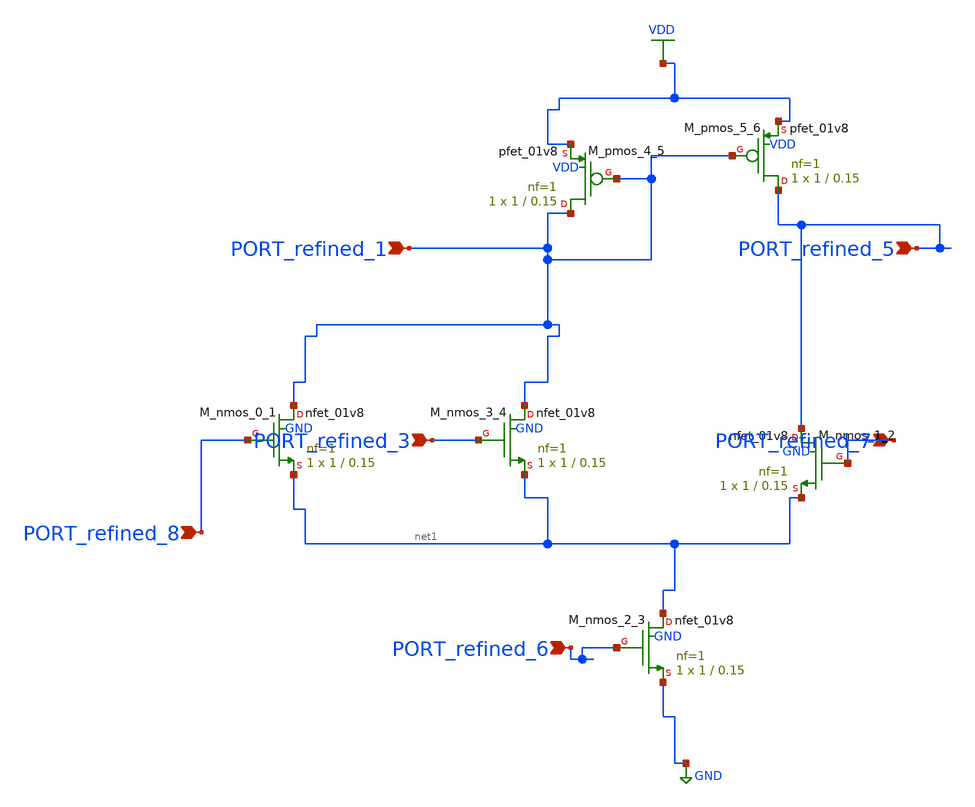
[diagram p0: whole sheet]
** sch_path: schematics/SchemGen/10_1109_TCSI_2022_3216201_04_001_crop1.sch
**.subckt 10_1109_TCSI_2022_3216201_04_001_crop1 PORT_refined_5 PORT_refined_6 PORT_refined_1
*+ PORT_refined_7 PORT_refined_8 PORT_refined_3
*.ipin PORT_refined_5
*.ipin PORT_refined_6
*.ipin PORT_refined_1
*.ipin PORT_refined_7
*.ipin PORT_refined_8
*.ipin PORT_refined_3
XM_nmos_0_1 PORT_refined_1 PORT_refined_8 net1 GND sky130_fd_pr__nfet_01v8 L=0.15 W=1 nf=1 ad='int((1 + 1)/2) * 1 / 1 * 0.29'
+ as='int((1 + 2)/2) * 1 / 1 * 0.29' pd='2*int((1 + 1)/2) * (1 / 1 + 0.29)' ps='2*int((1 + 2)/2) * (1 / 1 + 0.29)'
+ nrd='0.29 / 1 ' nrs='0.29 / 1 ' sa=0 sb=0 sd=0 mult=1 m=1
XM_nmos_1_2 PORT_refined_5 PORT_refined_7 net1 GND sky130_fd_pr__nfet_01v8 L=0.15 W=1 nf=1 ad='int((1 + 1)/2) * 1 / 1 * 0.29'
+ as='int((1 + 2)/2) * 1 / 1 * 0.29' pd='2*int((1 + 1)/2) * (1 / 1 + 0.29)' ps='2*int((1 + 2)/2) * (1 / 1 + 0.29)'
+ nrd='0.29 / 1 ' nrs='0.29 / 1 ' sa=0 sb=0 sd=0 mult=1 m=1
XM_nmos_2_3 net1 PORT_refined_6 GND GND sky130_fd_pr__nfet_01v8 L=0.15 W=1 nf=1 ad='int((1 + 1)/2) * 1 / 1 * 0.29'
+ as='int((1 + 2)/2) * 1 / 1 * 0.29' pd='2*int((1 + 1)/2) * (1 / 1 + 0.29)' ps='2*int((1 + 2)/2) * (1 / 1 + 0.29)'
+ nrd='0.29 / 1 ' nrs='0.29 / 1 ' sa=0 sb=0 sd=0 mult=1 m=1
XM_nmos_3_4 PORT_refined_1 PORT_refined_3 net1 GND sky130_fd_pr__nfet_01v8 L=0.15 W=1 nf=1 ad='int((1 + 1)/2) * 1 / 1 * 0.29'
+ as='int((1 + 2)/2) * 1 / 1 * 0.29' pd='2*int((1 + 1)/2) * (1 / 1 + 0.29)' ps='2*int((1 + 2)/2) * (1 / 1 + 0.29)'
+ nrd='0.29 / 1 ' nrs='0.29 / 1 ' sa=0 sb=0 sd=0 mult=1 m=1
XM_pmos_4_5 PORT_refined_1 PORT_refined_1 VDD VDD sky130_fd_pr__pfet_01v8 L=0.15 W=1 nf=1 ad='int((1 + 1)/2) * 1 / 1 * 0.29'
+ as='int((1 + 2)/2) * 1 / 1 * 0.29' pd='2*int((1 + 1)/2) * (1 / 1 + 0.29)' ps='2*int((1 + 2)/2) * (1 / 1 + 0.29)'
+ nrd='0.29 / 1 ' nrs='0.29 / 1 ' sa=0 sb=0 sd=0 mult=1 m=1
XM_pmos_5_6 PORT_refined_5 PORT_refined_1 VDD VDD sky130_fd_pr__pfet_01v8 L=0.15 W=1 nf=1 ad='int((1 + 1)/2) * 1 / 1 * 0.29'
+ as='int((1 + 2)/2) * 1 / 1 * 0.29' pd='2*int((1 + 1)/2) * (1 / 1 + 0.29)' ps='2*int((1 + 2)/2) * (1 / 1 + 0.29)'
+ nrd='0.29 / 1 ' nrs='0.29 / 1 ' sa=0 sb=0 sd=0 mult=1 m=1
**.ends
.GLOBAL GND
.GLOBAL VDD
.end
